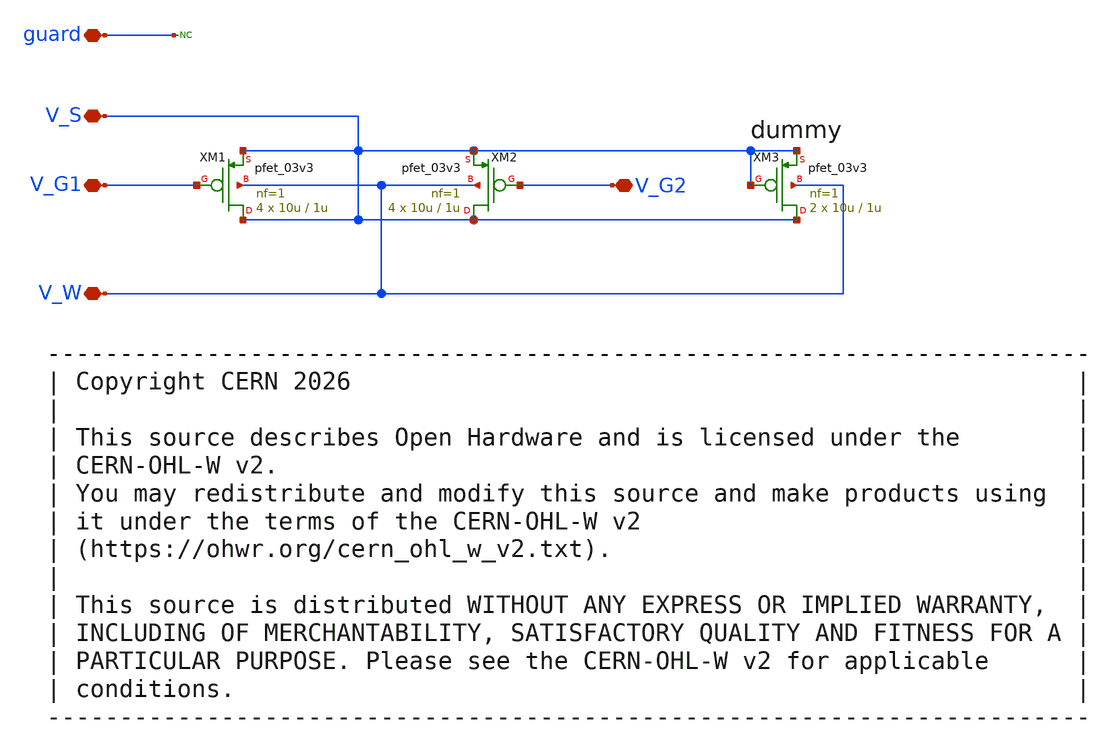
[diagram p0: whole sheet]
** sch_path: xschem/matched_interface_trap_charge_pumps.sch
* SPDX-FileCopyrightText: 2026 CERN
* SPDX-License-Identifier: CERN-OHL-W-2.0
* Copyright CERN 2026
* This source describes Open Hardware and is licensed under the
* CERN-OHL-W v2.
**.subckt matched_interface_trap_charge_pumps guard V_W V_S V_G1 V_G2
*.iopin guard
*.iopin V_W
*.iopin V_S
*.iopin V_G1
*.iopin V_G2
XM1 V_S V_G1 V_S V_W pfet_03v3 L=1u W=10u nf=1 ad='int((nf+1)/2) * W/nf * 0.18u' as='int((nf+2)/2) * W/nf * 0.18u'
+ pd='2*int((nf+1)/2) * (W/nf + 0.18u)' ps='2*int((nf+2)/2) * (W/nf + 0.18u)' nrd='0.18u / W' nrs='0.18u / W'
+ sa=0 sb=0 sd=0 m=4
XM2 V_S V_G2 V_S V_W pfet_03v3 L=1u W=10u nf=1 ad='int((nf+1)/2) * W/nf * 0.18u' as='int((nf+2)/2) * W/nf * 0.18u'
+ pd='2*int((nf+1)/2) * (W/nf + 0.18u)' ps='2*int((nf+2)/2) * (W/nf + 0.18u)' nrd='0.18u / W' nrs='0.18u / W'
+ sa=0 sb=0 sd=0 m=4
* noconn guard
XM3 V_S V_S V_S V_W pfet_03v3 L=1u W=10u nf=1 ad='int((nf+1)/2) * W/nf * 0.18u' as='int((nf+2)/2) * W/nf * 0.18u'
+ pd='2*int((nf+1)/2) * (W/nf + 0.18u)' ps='2*int((nf+2)/2) * (W/nf + 0.18u)' nrd='0.18u / W' nrs='0.18u / W'
+ sa=0 sb=0 sd=0 m=2
**.ends
.end
